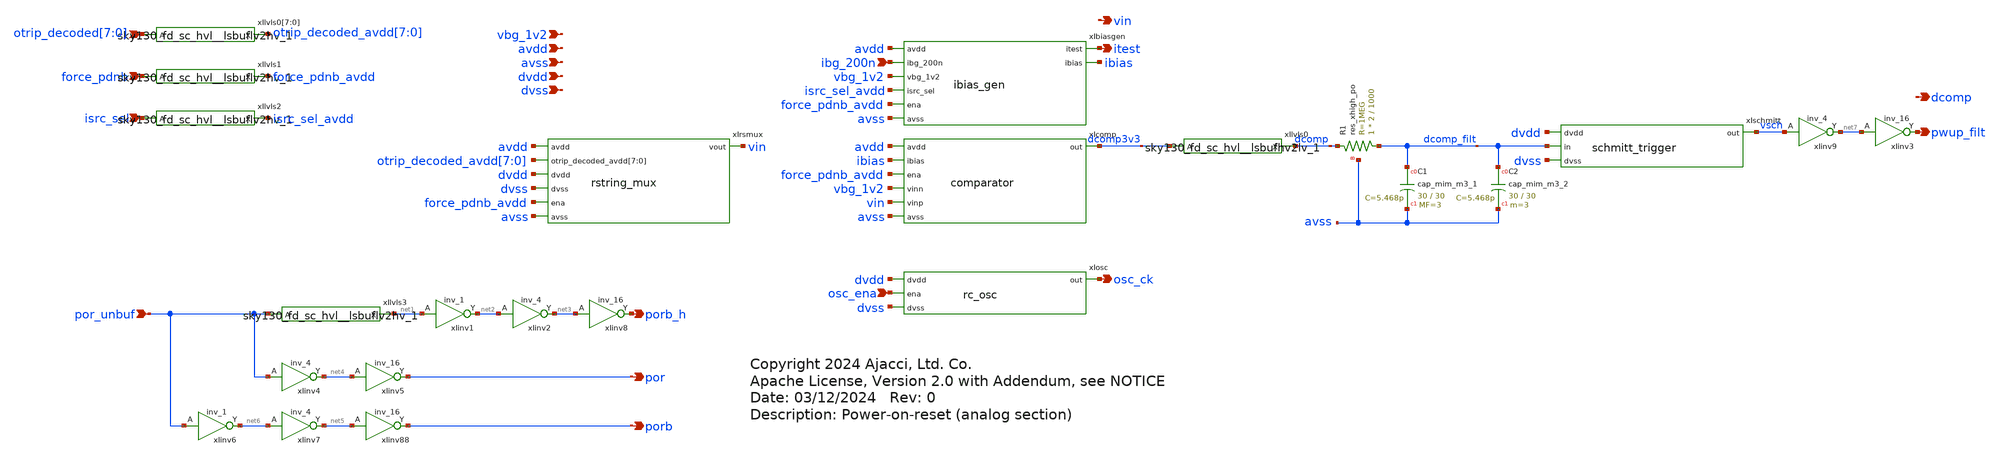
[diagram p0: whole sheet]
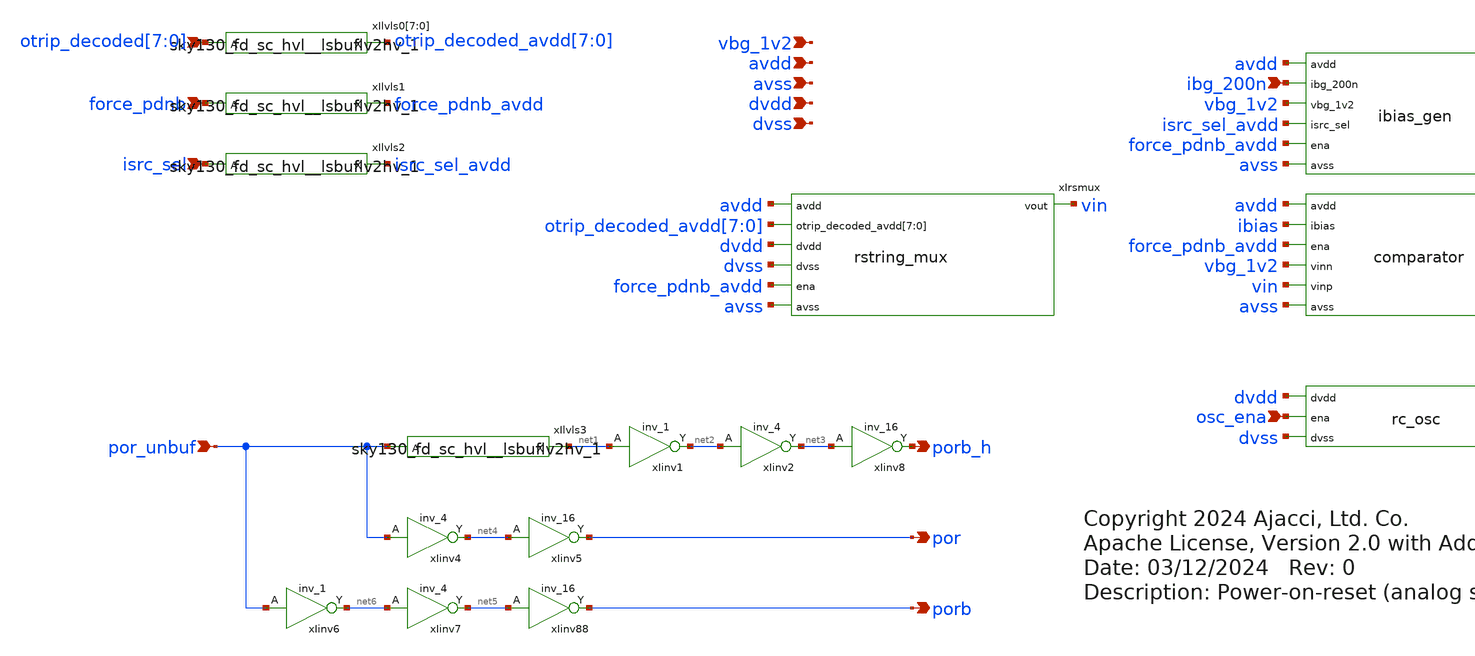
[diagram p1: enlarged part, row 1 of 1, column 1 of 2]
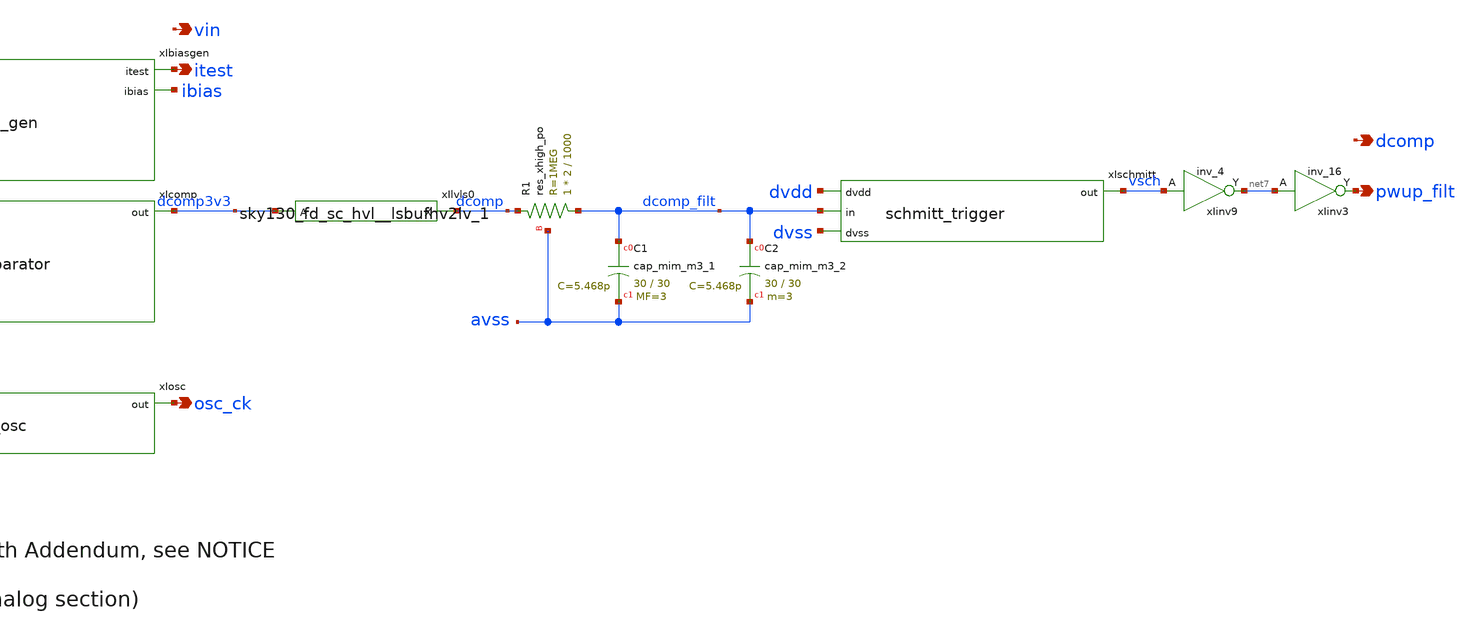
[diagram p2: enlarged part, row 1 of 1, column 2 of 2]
** sch_path: xschem/por_ana.sch
* Copyright 2024 Ajacci, Ltd. Co.
* Apache License, Version 2.0 with Addendum, see NOTICE
**.subckt por_ana vbg_1v2 avdd avss dvdd dvss force_pdnb isrc_sel ibg_200n pwup_filt itest osc_ena
*+ osc_ck
*+ otrip_decoded[7],otrip_decoded[6],otrip_decoded[5],otrip_decoded[4],otrip_decoded[3],otrip_decoded[2],otrip_decoded[1],otrip_decoded[0] vin por_unbuf porb_h por porb dcomp
*.ipin vbg_1v2
*.ipin avdd
*.ipin avss
*.ipin dvdd
*.ipin dvss
*.ipin force_pdnb
*.ipin isrc_sel
*.ipin ibg_200n
*.opin pwup_filt
*.opin itest
*.ipin osc_ena
*.opin osc_ck
*.ipin
*+ otrip_decoded[7],otrip_decoded[6],otrip_decoded[5],otrip_decoded[4],otrip_decoded[3],otrip_decoded[2],otrip_decoded[1],otrip_decoded[0]
*.opin vin
*.ipin por_unbuf
*.opin porb_h
*.opin por
*.opin porb
*.opin dcomp
XR1 dcomp_filt dcomp avss sky130_fd_pr__res_xhigh_po W=2 L=1000 mult=1 m=1
xIlvls0 dcomp3v3 dvdd avss avss avdd avdd dcomp sky130_fd_sc_hvl__lsbufhv2lv_1
XC1 dcomp_filt avss sky130_fd_pr__cap_mim_m3_1 W=30 L=30 MF=3 m=3
XC2 dcomp_filt avss sky130_fd_pr__cap_mim_m3_2 W=30 L=30 MF=3 m=3
xIlvls0[7] otrip_decoded[7] dvdd avss avss avdd avdd otrip_decoded_avdd[7]
+ sky130_fd_sc_hvl__lsbuflv2hv_1
xIlvls0[6] otrip_decoded[6] dvdd avss avss avdd avdd otrip_decoded_avdd[6]
+ sky130_fd_sc_hvl__lsbuflv2hv_1
xIlvls0[5] otrip_decoded[5] dvdd avss avss avdd avdd otrip_decoded_avdd[5]
+ sky130_fd_sc_hvl__lsbuflv2hv_1
xIlvls0[4] otrip_decoded[4] dvdd avss avss avdd avdd otrip_decoded_avdd[4]
+ sky130_fd_sc_hvl__lsbuflv2hv_1
xIlvls0[3] otrip_decoded[3] dvdd avss avss avdd avdd otrip_decoded_avdd[3]
+ sky130_fd_sc_hvl__lsbuflv2hv_1
xIlvls0[2] otrip_decoded[2] dvdd avss avss avdd avdd otrip_decoded_avdd[2]
+ sky130_fd_sc_hvl__lsbuflv2hv_1
xIlvls0[1] otrip_decoded[1] dvdd avss avss avdd avdd otrip_decoded_avdd[1]
+ sky130_fd_sc_hvl__lsbuflv2hv_1
xIlvls0[0] otrip_decoded[0] dvdd avss avss avdd avdd otrip_decoded_avdd[0]
+ sky130_fd_sc_hvl__lsbuflv2hv_1
xIlvls1 force_pdnb dvdd avss avss avdd avdd force_pdnb_avdd sky130_fd_sc_hvl__lsbuflv2hv_1
xIlvls2 isrc_sel dvdd avss avss avdd avdd isrc_sel_avdd sky130_fd_sc_hvl__lsbuflv2hv_1
xIrsmux avdd vin otrip_decoded_avdd[7] otrip_decoded_avdd[6] otrip_decoded_avdd[5]
+ otrip_decoded_avdd[4] otrip_decoded_avdd[3] otrip_decoded_avdd[2] otrip_decoded_avdd[1] otrip_decoded_avdd[0] dvdd dvss
+ force_pdnb_avdd avss rstring_mux
xIcomp avdd ibias dcomp3v3 force_pdnb_avdd vbg_1v2 vin avss comparator
xIbiasgen avdd itest ibias ibg_200n vbg_1v2 isrc_sel_avdd force_pdnb_avdd avss ibias_gen
xIosc dvdd osc_ck osc_ena dvss rc_osc
xIlvls3 por_unbuf dvdd avss avss avdd avdd net1 sky130_fd_sc_hvl__lsbuflv2hv_1
xIinv4 por_unbuf dvss dvss dvdd dvdd net4 sky130_fd_sc_hd__inv_4
xIinv5 net4 dvss dvss dvdd dvdd por sky130_fd_sc_hd__inv_16
xIinv7 net6 dvss dvss dvdd dvdd net5 sky130_fd_sc_hd__inv_4
xIinv88 net5 dvss dvss dvdd dvdd porb sky130_fd_sc_hd__inv_16
xIinv6 por_unbuf dvss dvss dvdd dvdd net6 sky130_fd_sc_hd__inv_1
xIinv8 net3 avss avss avdd avdd porb_h sky130_fd_sc_hvl__inv_16
xIinv2 net2 avss avss avdd avdd net3 sky130_fd_sc_hvl__inv_4
xIinv1 net1 avss avss avdd avdd net2 sky130_fd_sc_hvl__inv_1
xIschmitt dvdd dcomp_filt vsch dvss schmitt_trigger
xIinv3 net7 dvss dvss dvdd dvdd pwup_filt sky130_fd_sc_hd__inv_16
xIinv9 vsch dvss dvss dvdd dvdd net7 sky130_fd_sc_hvl__inv_4
**.ends

* expanding   symbol:  rstring_mux.sym # of pins=7
** sym_path: xschem/rstring_mux.sym
** sch_path: xschem/rstring_mux.sch
.subckt rstring_mux avdd vout otrip_decoded_avdd[7] otrip_decoded_avdd[6] otrip_decoded_avdd[5]
+ otrip_decoded_avdd[4] otrip_decoded_avdd[3] otrip_decoded_avdd[2] otrip_decoded_avdd[1] otrip_decoded_avdd[0] dvdd dvss
+ ena avss
*.ipin avdd
*.ipin avss
*.opin vout
*.ipin
*+ otrip_decoded_avdd[7],otrip_decoded_avdd[6],otrip_decoded_avdd[5],otrip_decoded_avdd[4],otrip_decoded_avdd[3],otrip_decoded_avdd[2],otrip_decoded_avdd[1],otrip_decoded_avdd[0]
*.ipin dvss
*.ipin dvdd
*.ipin ena
XR1 net2 net3 avss sky130_fd_pr__res_xhigh_po W=2 L=50 mult=1 m=1
XR2 net3 net4 avss sky130_fd_pr__res_xhigh_po W=2 L=50 mult=1 m=1
XR0 avss net2 avss sky130_fd_pr__res_xhigh_po W=2 L=50 mult=1 m=1
XR3 net4 net5 avss sky130_fd_pr__res_xhigh_po W=2 L=50 mult=1 m=1
XR4 net5 net6 avss sky130_fd_pr__res_xhigh_po W=2 L=50 mult=1 m=1
XR5 net6 net7 avss sky130_fd_pr__res_xhigh_po W=2 L=50 mult=1 m=1
XR6 net7 net8 avss sky130_fd_pr__res_xhigh_po W=2 L=50 mult=1 m=1
XR7 net8 net9 avss sky130_fd_pr__res_xhigh_po W=2 L=50 mult=1 m=1
XR8 net9 net10 avss sky130_fd_pr__res_xhigh_po W=2 L=50 mult=1 m=1
XR9 net10 net11 avss sky130_fd_pr__res_xhigh_po W=2 L=50 mult=1 m=1
XR10 net11 net12 avss sky130_fd_pr__res_xhigh_po W=2 L=50 mult=1 m=1
XR11 net12 net13 avss sky130_fd_pr__res_xhigh_po W=2 L=50 mult=1 m=1
XR12 net13 net14 avss sky130_fd_pr__res_xhigh_po W=2 L=50 mult=1 m=1
XR13 net14 net15 avss sky130_fd_pr__res_xhigh_po W=2 L=50 mult=1 m=1
XR14 net15 net16 avss sky130_fd_pr__res_xhigh_po W=2 L=50 mult=1 m=1
XR15 net16 net17 avss sky130_fd_pr__res_xhigh_po W=2 L=50 mult=1 m=1
XR16 net17 net18 avss sky130_fd_pr__res_xhigh_po W=2 L=50 mult=1 m=1
XR17 net18 net19 avss sky130_fd_pr__res_xhigh_po W=2 L=50 mult=1 m=1
XR18 net19 net20 avss sky130_fd_pr__res_xhigh_po W=2 L=50 mult=1 m=1
XR19 net20 net21 avss sky130_fd_pr__res_xhigh_po W=2 L=50 mult=1 m=1
XR20 net21 net22 avss sky130_fd_pr__res_xhigh_po W=2 L=50 mult=1 m=1
XR21 net22 net23 avss sky130_fd_pr__res_xhigh_po W=2 L=50 mult=1 m=1
XR22 net23 net24 avss sky130_fd_pr__res_xhigh_po W=2 L=50 mult=1 m=1
XR23 net24 net25 avss sky130_fd_pr__res_xhigh_po W=2 L=50 mult=1 m=1
XR24 net25 net26 avss sky130_fd_pr__res_xhigh_po W=2 L=50 mult=1 m=1
XR25 net26 net27 avss sky130_fd_pr__res_xhigh_po W=2 L=50 mult=1 m=1
XR26 net27 net28 avss sky130_fd_pr__res_xhigh_po W=2 L=50 mult=1 m=1
XR27 net28 vtrip7 avss sky130_fd_pr__res_xhigh_po W=2 L=50 mult=1 m=1
XR28 vtrip7 vtrip6 avss sky130_fd_pr__res_xhigh_po W=2 L=50 mult=1 m=1
XR29 vtrip6 vtrip5 avss sky130_fd_pr__res_xhigh_po W=2 L=50 mult=1 m=1
XR30 vtrip5 vtrip4 avss sky130_fd_pr__res_xhigh_po W=2 L=50 mult=1 m=1
XR31 vtrip4 vtrip3 avss sky130_fd_pr__res_xhigh_po W=2 L=50 mult=1 m=1
XR32 vtrip3 vtrip2 avss sky130_fd_pr__res_xhigh_po W=2 L=50 mult=1 m=1
XR33 vtrip2 vtrip1 avss sky130_fd_pr__res_xhigh_po W=2 L=50 mult=1 m=1
XR34 vtrip1 vtrip0 avss sky130_fd_pr__res_xhigh_po W=2 L=50 mult=1 m=1
XR35 vtrip0 net29 avss sky130_fd_pr__res_xhigh_po W=2 L=50 mult=1 m=1
XR36 net29 net30 avss sky130_fd_pr__res_xhigh_po W=2 L=50 mult=1 m=1
XR37 net30 net31 avss sky130_fd_pr__res_xhigh_po W=2 L=50 mult=1 m=1
XR38 net31 net32 avss sky130_fd_pr__res_xhigh_po W=2 L=50 mult=1 m=1
XR39 net32 net33 avss sky130_fd_pr__res_xhigh_po W=2 L=50 mult=1 m=1
XR40 net33 net34 avss sky130_fd_pr__res_xhigh_po W=2 L=50 mult=1 m=1
XR41 net34 net35 avss sky130_fd_pr__res_xhigh_po W=2 L=50 mult=1 m=1
XR42 net35 net36 avss sky130_fd_pr__res_xhigh_po W=2 L=50 mult=1 m=1
XR43 net36 net37 avss sky130_fd_pr__res_xhigh_po W=2 L=50 mult=1 m=1
XR44 net37 net38 avss sky130_fd_pr__res_xhigh_po W=2 L=50 mult=1 m=1
XR45 net38 net39 avss sky130_fd_pr__res_xhigh_po W=2 L=50 mult=1 m=1
XR46 net39 net40 avss sky130_fd_pr__res_xhigh_po W=2 L=50 mult=1 m=1
XR47 net40 net41 avss sky130_fd_pr__res_xhigh_po W=2 L=50 mult=1 m=1
XR48 net41 net42 avss sky130_fd_pr__res_xhigh_po W=2 L=50 mult=1 m=1
XR49 net42 net43 avss sky130_fd_pr__res_xhigh_po W=2 L=50 mult=1 m=1
XR50 net43 net44 avss sky130_fd_pr__res_xhigh_po W=2 L=50 mult=1 m=1
XR51 net44 net45 avss sky130_fd_pr__res_xhigh_po W=2 L=50 mult=1 m=1
XR52 net45 net46 avss sky130_fd_pr__res_xhigh_po W=2 L=50 mult=1 m=1
XR53 net46 net47 avss sky130_fd_pr__res_xhigh_po W=2 L=50 mult=1 m=1
XR54 net47 net48 avss sky130_fd_pr__res_xhigh_po W=2 L=50 mult=1 m=1
XR55 net48 net49 avss sky130_fd_pr__res_xhigh_po W=2 L=50 mult=1 m=1
XR56 net49 net50 avss sky130_fd_pr__res_xhigh_po W=2 L=50 mult=1 m=1
XR57 net50 net51 avss sky130_fd_pr__res_xhigh_po W=2 L=50 mult=1 m=1
XR58 net51 net52 avss sky130_fd_pr__res_xhigh_po W=2 L=50 mult=1 m=1
XR59 net52 net53 avss sky130_fd_pr__res_xhigh_po W=2 L=50 mult=1 m=1
XR60 net53 net54 avss sky130_fd_pr__res_xhigh_po W=2 L=50 mult=1 m=1
XR61 net54 net55 avss sky130_fd_pr__res_xhigh_po W=2 L=50 mult=1 m=1
XR62 net55 net56 avss sky130_fd_pr__res_xhigh_po W=2 L=50 mult=1 m=1
XR63 net56 net57 avss sky130_fd_pr__res_xhigh_po W=2 L=50 mult=1 m=1
XR64 net57 net58 avss sky130_fd_pr__res_xhigh_po W=2 L=50 mult=1 m=1
XR65 net58 net59 avss sky130_fd_pr__res_xhigh_po W=2 L=50 mult=1 m=1
XR66 net59 net60 avss sky130_fd_pr__res_xhigh_po W=2 L=50 mult=1 m=1
XR67 net60 net61 avss sky130_fd_pr__res_xhigh_po W=2 L=50 mult=1 m=1
XR68 net61 net62 avss sky130_fd_pr__res_xhigh_po W=2 L=50 mult=1 m=1
XR69 net62 net1 avss sky130_fd_pr__res_xhigh_po W=2 L=50 mult=1 m=1
XMtp[7] vtrip7 otrip_decoded_b_avdd[7] vout avdd sky130_fd_pr__pfet_g5v0d10v5 L=0.6 W=5 nf=1 ad='int((nf+1)/2) * W/nf * 0.29'
+ as='int((nf+2)/2) * W/nf * 0.29' pd='2*int((nf+1)/2) * (W/nf + 0.29)' ps='2*int((nf+2)/2) * (W/nf + 0.29)'
+ nrd='0.29 / W' nrs='0.29 / W' sa=0 sb=0 sd=0 mult=2 m=2
XMtp[6] vtrip6 otrip_decoded_b_avdd[6] vout avdd sky130_fd_pr__pfet_g5v0d10v5 L=0.6 W=5 nf=1 ad='int((nf+1)/2) * W/nf * 0.29'
+ as='int((nf+2)/2) * W/nf * 0.29' pd='2*int((nf+1)/2) * (W/nf + 0.29)' ps='2*int((nf+2)/2) * (W/nf + 0.29)'
+ nrd='0.29 / W' nrs='0.29 / W' sa=0 sb=0 sd=0 mult=2 m=2
XMtp[5] vtrip5 otrip_decoded_b_avdd[5] vout avdd sky130_fd_pr__pfet_g5v0d10v5 L=0.6 W=5 nf=1 ad='int((nf+1)/2) * W/nf * 0.29'
+ as='int((nf+2)/2) * W/nf * 0.29' pd='2*int((nf+1)/2) * (W/nf + 0.29)' ps='2*int((nf+2)/2) * (W/nf + 0.29)'
+ nrd='0.29 / W' nrs='0.29 / W' sa=0 sb=0 sd=0 mult=2 m=2
XMtp[4] vtrip4 otrip_decoded_b_avdd[4] vout avdd sky130_fd_pr__pfet_g5v0d10v5 L=0.6 W=5 nf=1 ad='int((nf+1)/2) * W/nf * 0.29'
+ as='int((nf+2)/2) * W/nf * 0.29' pd='2*int((nf+1)/2) * (W/nf + 0.29)' ps='2*int((nf+2)/2) * (W/nf + 0.29)'
+ nrd='0.29 / W' nrs='0.29 / W' sa=0 sb=0 sd=0 mult=2 m=2
XMtp[3] vtrip3 otrip_decoded_b_avdd[3] vout avdd sky130_fd_pr__pfet_g5v0d10v5 L=0.6 W=5 nf=1 ad='int((nf+1)/2) * W/nf * 0.29'
+ as='int((nf+2)/2) * W/nf * 0.29' pd='2*int((nf+1)/2) * (W/nf + 0.29)' ps='2*int((nf+2)/2) * (W/nf + 0.29)'
+ nrd='0.29 / W' nrs='0.29 / W' sa=0 sb=0 sd=0 mult=2 m=2
XMtp[2] vtrip2 otrip_decoded_b_avdd[2] vout avdd sky130_fd_pr__pfet_g5v0d10v5 L=0.6 W=5 nf=1 ad='int((nf+1)/2) * W/nf * 0.29'
+ as='int((nf+2)/2) * W/nf * 0.29' pd='2*int((nf+1)/2) * (W/nf + 0.29)' ps='2*int((nf+2)/2) * (W/nf + 0.29)'
+ nrd='0.29 / W' nrs='0.29 / W' sa=0 sb=0 sd=0 mult=2 m=2
XMtp[1] vtrip1 otrip_decoded_b_avdd[1] vout avdd sky130_fd_pr__pfet_g5v0d10v5 L=0.6 W=5 nf=1 ad='int((nf+1)/2) * W/nf * 0.29'
+ as='int((nf+2)/2) * W/nf * 0.29' pd='2*int((nf+1)/2) * (W/nf + 0.29)' ps='2*int((nf+2)/2) * (W/nf + 0.29)'
+ nrd='0.29 / W' nrs='0.29 / W' sa=0 sb=0 sd=0 mult=2 m=2
XMtp[0] vtrip0 otrip_decoded_b_avdd[0] vout avdd sky130_fd_pr__pfet_g5v0d10v5 L=0.6 W=5 nf=1 ad='int((nf+1)/2) * W/nf * 0.29'
+ as='int((nf+2)/2) * W/nf * 0.29' pd='2*int((nf+1)/2) * (W/nf + 0.29)' ps='2*int((nf+2)/2) * (W/nf + 0.29)'
+ nrd='0.29 / W' nrs='0.29 / W' sa=0 sb=0 sd=0 mult=2 m=2
XMtn[7] vout otrip_decoded_avdd[7] vtrip7 avss sky130_fd_pr__nfet_g5v0d10v5 L=0.6 W=5 nf=1 ad='int((nf+1)/2) * W/nf * 0.29'
+ as='int((nf+2)/2) * W/nf * 0.29' pd='2*int((nf+1)/2) * (W/nf + 0.29)' ps='2*int((nf+2)/2) * (W/nf + 0.29)'
+ nrd='0.29 / W' nrs='0.29 / W' sa=0 sb=0 sd=0 mult=2 m=2
XMtn[6] vout otrip_decoded_avdd[6] vtrip6 avss sky130_fd_pr__nfet_g5v0d10v5 L=0.6 W=5 nf=1 ad='int((nf+1)/2) * W/nf * 0.29'
+ as='int((nf+2)/2) * W/nf * 0.29' pd='2*int((nf+1)/2) * (W/nf + 0.29)' ps='2*int((nf+2)/2) * (W/nf + 0.29)'
+ nrd='0.29 / W' nrs='0.29 / W' sa=0 sb=0 sd=0 mult=2 m=2
XMtn[5] vout otrip_decoded_avdd[5] vtrip5 avss sky130_fd_pr__nfet_g5v0d10v5 L=0.6 W=5 nf=1 ad='int((nf+1)/2) * W/nf * 0.29'
+ as='int((nf+2)/2) * W/nf * 0.29' pd='2*int((nf+1)/2) * (W/nf + 0.29)' ps='2*int((nf+2)/2) * (W/nf + 0.29)'
+ nrd='0.29 / W' nrs='0.29 / W' sa=0 sb=0 sd=0 mult=2 m=2
XMtn[4] vout otrip_decoded_avdd[4] vtrip4 avss sky130_fd_pr__nfet_g5v0d10v5 L=0.6 W=5 nf=1 ad='int((nf+1)/2) * W/nf * 0.29'
+ as='int((nf+2)/2) * W/nf * 0.29' pd='2*int((nf+1)/2) * (W/nf + 0.29)' ps='2*int((nf+2)/2) * (W/nf + 0.29)'
+ nrd='0.29 / W' nrs='0.29 / W' sa=0 sb=0 sd=0 mult=2 m=2
XMtn[3] vout otrip_decoded_avdd[3] vtrip3 avss sky130_fd_pr__nfet_g5v0d10v5 L=0.6 W=5 nf=1 ad='int((nf+1)/2) * W/nf * 0.29'
+ as='int((nf+2)/2) * W/nf * 0.29' pd='2*int((nf+1)/2) * (W/nf + 0.29)' ps='2*int((nf+2)/2) * (W/nf + 0.29)'
+ nrd='0.29 / W' nrs='0.29 / W' sa=0 sb=0 sd=0 mult=2 m=2
XMtn[2] vout otrip_decoded_avdd[2] vtrip2 avss sky130_fd_pr__nfet_g5v0d10v5 L=0.6 W=5 nf=1 ad='int((nf+1)/2) * W/nf * 0.29'
+ as='int((nf+2)/2) * W/nf * 0.29' pd='2*int((nf+1)/2) * (W/nf + 0.29)' ps='2*int((nf+2)/2) * (W/nf + 0.29)'
+ nrd='0.29 / W' nrs='0.29 / W' sa=0 sb=0 sd=0 mult=2 m=2
XMtn[1] vout otrip_decoded_avdd[1] vtrip1 avss sky130_fd_pr__nfet_g5v0d10v5 L=0.6 W=5 nf=1 ad='int((nf+1)/2) * W/nf * 0.29'
+ as='int((nf+2)/2) * W/nf * 0.29' pd='2*int((nf+1)/2) * (W/nf + 0.29)' ps='2*int((nf+2)/2) * (W/nf + 0.29)'
+ nrd='0.29 / W' nrs='0.29 / W' sa=0 sb=0 sd=0 mult=2 m=2
XMtn[0] vout otrip_decoded_avdd[0] vtrip0 avss sky130_fd_pr__nfet_g5v0d10v5 L=0.6 W=5 nf=1 ad='int((nf+1)/2) * W/nf * 0.29'
+ as='int((nf+2)/2) * W/nf * 0.29' pd='2*int((nf+1)/2) * (W/nf + 0.29)' ps='2*int((nf+2)/2) * (W/nf + 0.29)'
+ nrd='0.29 / W' nrs='0.29 / W' sa=0 sb=0 sd=0 mult=2 m=2
XMpdn net1 ena_b avss avss sky130_fd_pr__nfet_g5v0d10v5 L=1 W=1 nf=1 ad='int((nf+1)/2) * W/nf * 0.29'
+ as='int((nf+2)/2) * W/nf * 0.29' pd='2*int((nf+1)/2) * (W/nf + 0.29)' ps='2*int((nf+2)/2) * (W/nf + 0.29)'
+ nrd='0.29 / W' nrs='0.29 / W' sa=0 sb=0 sd=0 mult=1 m=1
xIinv0[7] otrip_decoded_avdd[7] avss avss avdd avdd otrip_decoded_b_avdd[7] sky130_fd_sc_hvl__inv_1
xIinv0[6] otrip_decoded_avdd[6] avss avss avdd avdd otrip_decoded_b_avdd[6] sky130_fd_sc_hvl__inv_1
xIinv0[5] otrip_decoded_avdd[5] avss avss avdd avdd otrip_decoded_b_avdd[5] sky130_fd_sc_hvl__inv_1
xIinv0[4] otrip_decoded_avdd[4] avss avss avdd avdd otrip_decoded_b_avdd[4] sky130_fd_sc_hvl__inv_1
xIinv0[3] otrip_decoded_avdd[3] avss avss avdd avdd otrip_decoded_b_avdd[3] sky130_fd_sc_hvl__inv_1
xIinv0[2] otrip_decoded_avdd[2] avss avss avdd avdd otrip_decoded_b_avdd[2] sky130_fd_sc_hvl__inv_1
xIinv0[1] otrip_decoded_avdd[1] avss avss avdd avdd otrip_decoded_b_avdd[1] sky130_fd_sc_hvl__inv_1
xIinv0[0] otrip_decoded_avdd[0] avss avss avdd avdd otrip_decoded_b_avdd[0] sky130_fd_sc_hvl__inv_1
xIinv1 ena avss avss avdd avdd ena_b sky130_fd_sc_hvl__inv_1
XMpdp avdd ena_b net1 avdd sky130_fd_pr__pfet_g5v0d10v5 L=0.6 W=5 nf=1 ad='int((nf+1)/2) * W/nf * 0.29'
+ as='int((nf+2)/2) * W/nf * 0.29' pd='2*int((nf+1)/2) * (W/nf + 0.29)' ps='2*int((nf+2)/2) * (W/nf + 0.29)'
+ nrd='0.29 / W' nrs='0.29 / W' sa=0 sb=0 sd=0 mult=16 m=16
.ends


* expanding   symbol:  comparator.sym # of pins=7
** sym_path: xschem/comparator.sym
** sch_path: xschem/comparator.sch
.subckt comparator avdd ibias out ena vinn vinp avss
*.ipin ena
*.ipin avdd
*.ipin avss
*.ipin ibias
*.ipin vinn
*.ipin vinp
*.opin out
XMb vn vn avss avss sky130_fd_pr__nfet_g5v0d10v5 L=8 W=1 nf=1 ad='int((nf+1)/2) * W/nf * 0.29' as='int((nf+2)/2) * W/nf * 0.29'
+ pd='2*int((nf+1)/2) * (W/nf + 0.29)' ps='2*int((nf+2)/2) * (W/nf + 0.29)' nrd='0.29 / W' nrs='0.29 / W'
+ sa=0 sb=0 sd=0 mult=2 m=2
XMta vt vn avss avss sky130_fd_pr__nfet_g5v0d10v5 L=8 W=1 nf=1 ad='int((nf+1)/2) * W/nf * 0.29' as='int((nf+2)/2) * W/nf * 0.29'
+ pd='2*int((nf+1)/2) * (W/nf + 0.29)' ps='2*int((nf+2)/2) * (W/nf + 0.29)' nrd='0.29 / W' nrs='0.29 / W'
+ sa=0 sb=0 sd=0 mult=2 m=2
XMl0 vn ena_b avss avss sky130_fd_pr__nfet_g5v0d10v5 L=1 W=1 nf=1 ad='int((nf+1)/2) * W/nf * 0.29' as='int((nf+2)/2) * W/nf * 0.29'
+ pd='2*int((nf+1)/2) * (W/nf + 0.29)' ps='2*int((nf+2)/2) * (W/nf + 0.29)' nrd='0.29 / W' nrs='0.29 / W'
+ sa=0 sb=0 sd=0 mult=1 m=1
XMinv0 ena_b ena avss avss sky130_fd_pr__nfet_g5v0d10v5 L=1 W=1 nf=1 ad='int((nf+1)/2) * W/nf * 0.29'
+ as='int((nf+2)/2) * W/nf * 0.29' pd='2*int((nf+1)/2) * (W/nf + 0.29)' ps='2*int((nf+2)/2) * (W/nf + 0.29)'
+ nrd='0.29 / W' nrs='0.29 / W' sa=0 sb=0 sd=0 mult=1 m=1
XMinv1 ena_b ena avdd avdd sky130_fd_pr__pfet_g5v0d10v5 L=1 W=1 nf=1 ad='int((nf+1)/2) * W/nf * 0.29'
+ as='int((nf+2)/2) * W/nf * 0.29' pd='2*int((nf+1)/2) * (W/nf + 0.29)' ps='2*int((nf+2)/2) * (W/nf + 0.29)'
+ nrd='0.29 / W' nrs='0.29 / W' sa=0 sb=0 sd=0 mult=1 m=1
XMi0 vnn vinn vt vt sky130_fd_pr__nfet_g5v0d10v5 L=8 W=0.42 nf=1 ad='int((nf+1)/2) * W/nf * 0.29' as='int((nf+2)/2) * W/nf * 0.29'
+ pd='2*int((nf+1)/2) * (W/nf + 0.29)' ps='2*int((nf+2)/2) * (W/nf + 0.29)' nrd='0.29 / W' nrs='0.29 / W'
+ sa=0 sb=0 sd=0 mult=16 m=16
XMi1 vpp vinp vt vt sky130_fd_pr__nfet_g5v0d10v5 L=8 W=0.42 nf=1 ad='int((nf+1)/2) * W/nf * 0.29' as='int((nf+2)/2) * W/nf * 0.29'
+ pd='2*int((nf+1)/2) * (W/nf + 0.29)' ps='2*int((nf+2)/2) * (W/nf + 0.29)' nrd='0.29 / W' nrs='0.29 / W'
+ sa=0 sb=0 sd=0 mult=16 m=16
XMld1 vpp vpp avdd avdd sky130_fd_pr__pfet_g5v0d10v5 L=8 W=0.42 nf=1 ad='int((nf+1)/2) * W/nf * 0.29'
+ as='int((nf+2)/2) * W/nf * 0.29' pd='2*int((nf+1)/2) * (W/nf + 0.29)' ps='2*int((nf+2)/2) * (W/nf + 0.29)'
+ nrd='0.29 / W' nrs='0.29 / W' sa=0 sb=0 sd=0 mult=8 m=8
XMh1 vnn vpp avdd avdd sky130_fd_pr__pfet_g5v0d10v5 L=8 W=0.42 nf=1 ad='int((nf+1)/2) * W/nf * 0.29'
+ as='int((nf+2)/2) * W/nf * 0.29' pd='2*int((nf+1)/2) * (W/nf + 0.29)' ps='2*int((nf+2)/2) * (W/nf + 0.29)'
+ nrd='0.29 / W' nrs='0.29 / W' sa=0 sb=0 sd=0 mult=14 m=14
XMh0 vpp vnn avdd avdd sky130_fd_pr__pfet_g5v0d10v5 L=8 W=0.42 nf=1 ad='int((nf+1)/2) * W/nf * 0.29'
+ as='int((nf+2)/2) * W/nf * 0.29' pd='2*int((nf+1)/2) * (W/nf + 0.29)' ps='2*int((nf+2)/2) * (W/nf + 0.29)'
+ nrd='0.29 / W' nrs='0.29 / W' sa=0 sb=0 sd=0 mult=14 m=14
XMld0 vnn vnn avdd avdd sky130_fd_pr__pfet_g5v0d10v5 L=8 W=0.42 nf=1 ad='int((nf+1)/2) * W/nf * 0.29'
+ as='int((nf+2)/2) * W/nf * 0.29' pd='2*int((nf+1)/2) * (W/nf + 0.29)' ps='2*int((nf+2)/2) * (W/nf + 0.29)'
+ nrd='0.29 / W' nrs='0.29 / W' sa=0 sb=0 sd=0 mult=8 m=8
XMpp1 n0 vpp avdd avdd sky130_fd_pr__pfet_g5v0d10v5 L=8 W=1 nf=1 ad='int((nf+1)/2) * W/nf * 0.29' as='int((nf+2)/2) * W/nf * 0.29'
+ pd='2*int((nf+1)/2) * (W/nf + 0.29)' ps='2*int((nf+2)/2) * (W/nf + 0.29)' nrd='0.29 / W' nrs='0.29 / W'
+ sa=0 sb=0 sd=0 mult=2 m=2
XMnn1 n0 vm avss avss sky130_fd_pr__nfet_g5v0d10v5 L=8 W=1 nf=1 ad='int((nf+1)/2) * W/nf * 0.29' as='int((nf+2)/2) * W/nf * 0.29'
+ pd='2*int((nf+1)/2) * (W/nf + 0.29)' ps='2*int((nf+2)/2) * (W/nf + 0.29)' nrd='0.29 / W' nrs='0.29 / W'
+ sa=0 sb=0 sd=0 mult=2 m=2
XMpp0 vm vnn avdd avdd sky130_fd_pr__pfet_g5v0d10v5 L=8 W=1 nf=1 ad='int((nf+1)/2) * W/nf * 0.29' as='int((nf+2)/2) * W/nf * 0.29'
+ pd='2*int((nf+1)/2) * (W/nf + 0.29)' ps='2*int((nf+2)/2) * (W/nf + 0.29)' nrd='0.29 / W' nrs='0.29 / W'
+ sa=0 sb=0 sd=0 mult=2 m=2
XMnn0 vm vm avss avss sky130_fd_pr__nfet_g5v0d10v5 L=8 W=1 nf=1 ad='int((nf+1)/2) * W/nf * 0.29' as='int((nf+2)/2) * W/nf * 0.29'
+ pd='2*int((nf+1)/2) * (W/nf + 0.29)' ps='2*int((nf+2)/2) * (W/nf + 0.29)' nrd='0.29 / W' nrs='0.29 / W'
+ sa=0 sb=0 sd=0 mult=2 m=2
XMinv3 n1 n0 avdd avdd sky130_fd_pr__pfet_g5v0d10v5 L=0.6 W=1 nf=1 ad='int((nf+1)/2) * W/nf * 0.29' as='int((nf+2)/2) * W/nf * 0.29'
+ pd='2*int((nf+1)/2) * (W/nf + 0.29)' ps='2*int((nf+2)/2) * (W/nf + 0.29)' nrd='0.29 / W' nrs='0.29 / W'
+ sa=0 sb=0 sd=0 mult=2 m=2
XMinv2 n1 n0 avss avss sky130_fd_pr__nfet_g5v0d10v5 L=0.6 W=1 nf=1 ad='int((nf+1)/2) * W/nf * 0.29' as='int((nf+2)/2) * W/nf * 0.29'
+ pd='2*int((nf+1)/2) * (W/nf + 0.29)' ps='2*int((nf+2)/2) * (W/nf + 0.29)' nrd='0.29 / W' nrs='0.29 / W'
+ sa=0 sb=0 sd=0 mult=2 m=2
XMinv5 out n1 avdd avdd sky130_fd_pr__pfet_g5v0d10v5 L=0.6 W=1 nf=1 ad='int((nf+1)/2) * W/nf * 0.29'
+ as='int((nf+2)/2) * W/nf * 0.29' pd='2*int((nf+1)/2) * (W/nf + 0.29)' ps='2*int((nf+2)/2) * (W/nf + 0.29)'
+ nrd='0.29 / W' nrs='0.29 / W' sa=0 sb=0 sd=0 mult=8 m=8
XMinv4 out n1 avss avss sky130_fd_pr__nfet_g5v0d10v5 L=0.6 W=1 nf=1 ad='int((nf+1)/2) * W/nf * 0.29'
+ as='int((nf+2)/2) * W/nf * 0.29' pd='2*int((nf+1)/2) * (W/nf + 0.29)' ps='2*int((nf+2)/2) * (W/nf + 0.29)'
+ nrd='0.29 / W' nrs='0.29 / W' sa=0 sb=0 sd=0 mult=8 m=8
XMl1 vm ena_b avss avss sky130_fd_pr__nfet_g5v0d10v5 L=1 W=1 nf=1 ad='int((nf+1)/2) * W/nf * 0.29' as='int((nf+2)/2) * W/nf * 0.29'
+ pd='2*int((nf+1)/2) * (W/nf + 0.29)' ps='2*int((nf+2)/2) * (W/nf + 0.29)' nrd='0.29 / W' nrs='0.29 / W'
+ sa=0 sb=0 sd=0 mult=1 m=1
XMl3 vnn ena avdd avdd sky130_fd_pr__pfet_g5v0d10v5 L=1 W=1 nf=1 ad='int((nf+1)/2) * W/nf * 0.29' as='int((nf+2)/2) * W/nf * 0.29'
+ pd='2*int((nf+1)/2) * (W/nf + 0.29)' ps='2*int((nf+2)/2) * (W/nf + 0.29)' nrd='0.29 / W' nrs='0.29 / W'
+ sa=0 sb=0 sd=0 mult=1 m=1
XMl4 vpp ena avdd avdd sky130_fd_pr__pfet_g5v0d10v5 L=1 W=1 nf=1 ad='int((nf+1)/2) * W/nf * 0.29' as='int((nf+2)/2) * W/nf * 0.29'
+ pd='2*int((nf+1)/2) * (W/nf + 0.29)' ps='2*int((nf+2)/2) * (W/nf + 0.29)' nrd='0.29 / W' nrs='0.29 / W'
+ sa=0 sb=0 sd=0 mult=1 m=1
XMt1 ibias ena vn avss sky130_fd_pr__nfet_g5v0d10v5 L=1 W=1 nf=1 ad='int((nf+1)/2) * W/nf * 0.29' as='int((nf+2)/2) * W/nf * 0.29'
+ pd='2*int((nf+1)/2) * (W/nf + 0.29)' ps='2*int((nf+2)/2) * (W/nf + 0.29)' nrd='0.29 / W' nrs='0.29 / W'
+ sa=0 sb=0 sd=0 mult=1 m=1
XMt0 vn ena_b ibias avdd sky130_fd_pr__pfet_g5v0d10v5 L=1 W=1 nf=1 ad='int((nf+1)/2) * W/nf * 0.29' as='int((nf+2)/2) * W/nf * 0.29'
+ pd='2*int((nf+1)/2) * (W/nf + 0.29)' ps='2*int((nf+2)/2) * (W/nf + 0.29)' nrd='0.29 / W' nrs='0.29 / W'
+ sa=0 sb=0 sd=0 mult=1 m=1
XMl2 n0 ena_b avss avss sky130_fd_pr__nfet_g5v0d10v5 L=1 W=1 nf=1 ad='int((nf+1)/2) * W/nf * 0.29' as='int((nf+2)/2) * W/nf * 0.29'
+ pd='2*int((nf+1)/2) * (W/nf + 0.29)' ps='2*int((nf+2)/2) * (W/nf + 0.29)' nrd='0.29 / W' nrs='0.29 / W'
+ sa=0 sb=0 sd=0 mult=1 m=1
.ends


* expanding   symbol:  ibias_gen.sym # of pins=8
** sym_path: xschem/ibias_gen.sym
** sch_path: xschem/ibias_gen.sch
.subckt ibias_gen avdd itest ibias ibg_200n vbg_1v2 isrc_sel ena avss
*.ipin vbg_1v2
*.ipin ena
*.opin ibias
*.ipin ibg_200n
*.ipin isrc_sel
*.ipin avdd
*.ipin avss
*.opin itest
XR1 avss net3 avss sky130_fd_pr__res_xhigh_po W=2 L=1000 mult=1 m=1
XQ1 avss avss net2 sky130_fd_pr__pnp_05v5_W0p68L0p68 m=1
XM17 net1 vbg_1v2 vn0 avss sky130_fd_pr__nfet_g5v0d10v5 L=0.6 W=5 nf=1 ad='int((nf+1)/2) * W/nf * 0.29'
+ as='int((nf+2)/2) * W/nf * 0.29' pd='2*int((nf+1)/2) * (W/nf + 0.29)' ps='2*int((nf+2)/2) * (W/nf + 0.29)'
+ nrd='0.29 / W' nrs='0.29 / W' sa=0 sb=0 sd=0 mult=10 m=10
XMt9 net1 ena_b net4 avdd sky130_fd_pr__pfet_g5v0d10v5 L=0.6 W=5 nf=1 ad='int((nf+1)/2) * W/nf * 0.29'
+ as='int((nf+2)/2) * W/nf * 0.29' pd='2*int((nf+1)/2) * (W/nf + 0.29)' ps='2*int((nf+2)/2) * (W/nf + 0.29)'
+ nrd='0.29 / W' nrs='0.29 / W' sa=0 sb=0 sd=0 mult=1 m=1
XMn0 vn0 vn0 net2 avss sky130_fd_pr__nfet_g5v0d10v5 L=4 W=5 nf=1 ad='int((nf+1)/2) * W/nf * 0.29' as='int((nf+2)/2) * W/nf * 0.29'
+ pd='2*int((nf+1)/2) * (W/nf + 0.29)' ps='2*int((nf+2)/2) * (W/nf + 0.29)' nrd='0.29 / W' nrs='0.29 / W'
+ sa=0 sb=0 sd=0 mult=2 m=2
XMp0 vn0 vp0 avdd avdd sky130_fd_pr__pfet_g5v0d10v5 L=4 W=5 nf=1 ad='int((nf+1)/2) * W/nf * 0.29' as='int((nf+2)/2) * W/nf * 0.29'
+ pd='2*int((nf+1)/2) * (W/nf + 0.29)' ps='2*int((nf+2)/2) * (W/nf + 0.29)' nrd='0.29 / W' nrs='0.29 / W'
+ sa=0 sb=0 sd=0 mult=2 m=2
XMn1 vp0 vn0 net3 avss sky130_fd_pr__nfet_g5v0d10v5 L=4 W=5 nf=1 ad='int((nf+1)/2) * W/nf * 0.29' as='int((nf+2)/2) * W/nf * 0.29'
+ pd='2*int((nf+1)/2) * (W/nf + 0.29)' ps='2*int((nf+2)/2) * (W/nf + 0.29)' nrd='0.29 / W' nrs='0.29 / W'
+ sa=0 sb=0 sd=0 mult=2 m=2
XMp1 vp0 vp0 avdd avdd sky130_fd_pr__pfet_g5v0d10v5 L=4 W=5 nf=1 ad='int((nf+1)/2) * W/nf * 0.29' as='int((nf+2)/2) * W/nf * 0.29'
+ pd='2*int((nf+1)/2) * (W/nf + 0.29)' ps='2*int((nf+2)/2) * (W/nf + 0.29)' nrd='0.29 / W' nrs='0.29 / W'
+ sa=0 sb=0 sd=0 mult=2 m=2
XMp ibias vp avdd avdd sky130_fd_pr__pfet_g5v0d10v5 L=4 W=5 nf=1 ad='int((nf+1)/2) * W/nf * 0.29' as='int((nf+2)/2) * W/nf * 0.29'
+ pd='2*int((nf+1)/2) * (W/nf + 0.29)' ps='2*int((nf+2)/2) * (W/nf + 0.29)' nrd='0.29 / W' nrs='0.29 / W'
+ sa=0 sb=0 sd=0 mult=2 m=2
XMt0 vp0 isrc_sel vp avdd sky130_fd_pr__pfet_g5v0d10v5 L=0.6 W=5 nf=1 ad='int((nf+1)/2) * W/nf * 0.29'
+ as='int((nf+2)/2) * W/nf * 0.29' pd='2*int((nf+1)/2) * (W/nf + 0.29)' ps='2*int((nf+2)/2) * (W/nf + 0.29)'
+ nrd='0.29 / W' nrs='0.29 / W' sa=0 sb=0 sd=0 mult=1 m=1
XMt1 vp isrc_sel_b vp0 avss sky130_fd_pr__nfet_g5v0d10v5 L=0.6 W=5 nf=1 ad='int((nf+1)/2) * W/nf * 0.29'
+ as='int((nf+2)/2) * W/nf * 0.29' pd='2*int((nf+1)/2) * (W/nf + 0.29)' ps='2*int((nf+2)/2) * (W/nf + 0.29)'
+ nrd='0.29 / W' nrs='0.29 / W' sa=0 sb=0 sd=0 mult=1 m=1
XMl6 vp ena avdd avdd sky130_fd_pr__pfet_g5v0d10v5 L=2 W=5 nf=1 ad='int((nf+1)/2) * W/nf * 0.29' as='int((nf+2)/2) * W/nf * 0.29'
+ pd='2*int((nf+1)/2) * (W/nf + 0.29)' ps='2*int((nf+2)/2) * (W/nf + 0.29)' nrd='0.29 / W' nrs='0.29 / W'
+ sa=0 sb=0 sd=0 mult=1 m=1
XMl3 vp0 ena avdd avdd sky130_fd_pr__pfet_g5v0d10v5 L=2 W=5 nf=1 ad='int((nf+1)/2) * W/nf * 0.29' as='int((nf+2)/2) * W/nf * 0.29'
+ pd='2*int((nf+1)/2) * (W/nf + 0.29)' ps='2*int((nf+2)/2) * (W/nf + 0.29)' nrd='0.29 / W' nrs='0.29 / W'
+ sa=0 sb=0 sd=0 mult=1 m=1
XMl1 vn0 ena_b avss avss sky130_fd_pr__nfet_g5v0d10v5 L=2 W=5 nf=1 ad='int((nf+1)/2) * W/nf * 0.29' as='int((nf+2)/2) * W/nf * 0.29'
+ pd='2*int((nf+1)/2) * (W/nf + 0.29)' ps='2*int((nf+2)/2) * (W/nf + 0.29)' nrd='0.29 / W' nrs='0.29 / W'
+ sa=0 sb=0 sd=0 mult=1 m=1
XMnn1 vp1 vn1 avss avss sky130_fd_pr__nfet_g5v0d10v5 L=8 W=5 nf=1 ad='int((nf+1)/2) * W/nf * 0.29' as='int((nf+2)/2) * W/nf * 0.29'
+ pd='2*int((nf+1)/2) * (W/nf + 0.29)' ps='2*int((nf+2)/2) * (W/nf + 0.29)' nrd='0.29 / W' nrs='0.29 / W'
+ sa=0 sb=0 sd=0 mult=8 m=8
XMnn0 vn1 vn1 avss avss sky130_fd_pr__nfet_g5v0d10v5 L=8 W=5 nf=1 ad='int((nf+1)/2) * W/nf * 0.29' as='int((nf+2)/2) * W/nf * 0.29'
+ pd='2*int((nf+1)/2) * (W/nf + 0.29)' ps='2*int((nf+2)/2) * (W/nf + 0.29)' nrd='0.29 / W' nrs='0.29 / W'
+ sa=0 sb=0 sd=0 mult=2 m=2
XMl9 vn1 isrc_sel_b avss avss sky130_fd_pr__nfet_g5v0d10v5 L=2 W=5 nf=1 ad='int((nf+1)/2) * W/nf * 0.29'
+ as='int((nf+2)/2) * W/nf * 0.29' pd='2*int((nf+1)/2) * (W/nf + 0.29)' ps='2*int((nf+2)/2) * (W/nf + 0.29)'
+ nrd='0.29 / W' nrs='0.29 / W' sa=0 sb=0 sd=0 mult=1 m=1
XMt6 net5 isrc_sel vn1 avss sky130_fd_pr__nfet_g5v0d10v5 L=0.6 W=5 nf=1 ad='int((nf+1)/2) * W/nf * 0.29'
+ as='int((nf+2)/2) * W/nf * 0.29' pd='2*int((nf+1)/2) * (W/nf + 0.29)' ps='2*int((nf+2)/2) * (W/nf + 0.29)'
+ nrd='0.29 / W' nrs='0.29 / W' sa=0 sb=0 sd=0 mult=1 m=1
XMt7 vn1 isrc_sel_b net6 avdd sky130_fd_pr__pfet_g5v0d10v5 L=0.6 W=5 nf=1 ad='int((nf+1)/2) * W/nf * 0.29'
+ as='int((nf+2)/2) * W/nf * 0.29' pd='2*int((nf+1)/2) * (W/nf + 0.29)' ps='2*int((nf+2)/2) * (W/nf + 0.29)'
+ nrd='0.29 / W' nrs='0.29 / W' sa=0 sb=0 sd=0 mult=1 m=1
XMpp1 vp1 vp1 avdd avdd sky130_fd_pr__pfet_g5v0d10v5 L=4 W=5 nf=1 ad='int((nf+1)/2) * W/nf * 0.29' as='int((nf+2)/2) * W/nf * 0.29'
+ pd='2*int((nf+1)/2) * (W/nf + 0.29)' ps='2*int((nf+2)/2) * (W/nf + 0.29)' nrd='0.29 / W' nrs='0.29 / W'
+ sa=0 sb=0 sd=0 mult=2 m=2
XMt2 vp isrc_sel_b vp1 avdd sky130_fd_pr__pfet_g5v0d10v5 L=0.6 W=5 nf=1 ad='int((nf+1)/2) * W/nf * 0.29'
+ as='int((nf+2)/2) * W/nf * 0.29' pd='2*int((nf+1)/2) * (W/nf + 0.29)' ps='2*int((nf+2)/2) * (W/nf + 0.29)'
+ nrd='0.29 / W' nrs='0.29 / W' sa=0 sb=0 sd=0 mult=1 m=1
XMt3 vp1 isrc_sel vp avss sky130_fd_pr__nfet_g5v0d10v5 L=0.6 W=5 nf=1 ad='int((nf+1)/2) * W/nf * 0.29'
+ as='int((nf+2)/2) * W/nf * 0.29' pd='2*int((nf+1)/2) * (W/nf + 0.29)' ps='2*int((nf+2)/2) * (W/nf + 0.29)'
+ nrd='0.29 / W' nrs='0.29 / W' sa=0 sb=0 sd=0 mult=1 m=1
XMt4 ibg_200n ena net5 avss sky130_fd_pr__nfet_g5v0d10v5 L=0.6 W=5 nf=1 ad='int((nf+1)/2) * W/nf * 0.29'
+ as='int((nf+2)/2) * W/nf * 0.29' pd='2*int((nf+1)/2) * (W/nf + 0.29)' ps='2*int((nf+2)/2) * (W/nf + 0.29)'
+ nrd='0.29 / W' nrs='0.29 / W' sa=0 sb=0 sd=0 mult=1 m=1
XMt5 net6 ena_b ibg_200n avdd sky130_fd_pr__pfet_g5v0d10v5 L=0.6 W=5 nf=1 ad='int((nf+1)/2) * W/nf * 0.29'
+ as='int((nf+2)/2) * W/nf * 0.29' pd='2*int((nf+1)/2) * (W/nf + 0.29)' ps='2*int((nf+2)/2) * (W/nf + 0.29)'
+ nrd='0.29 / W' nrs='0.29 / W' sa=0 sb=0 sd=0 mult=1 m=1
XMl7 vp1 isrc_sel avdd avdd sky130_fd_pr__pfet_g5v0d10v5 L=2 W=5 nf=1 ad='int((nf+1)/2) * W/nf * 0.29'
+ as='int((nf+2)/2) * W/nf * 0.29' pd='2*int((nf+1)/2) * (W/nf + 0.29)' ps='2*int((nf+2)/2) * (W/nf + 0.29)'
+ nrd='0.29 / W' nrs='0.29 / W' sa=0 sb=0 sd=0 mult=1 m=1
XMl8 vp1 ena avdd avdd sky130_fd_pr__pfet_g5v0d10v5 L=2 W=5 nf=1 ad='int((nf+1)/2) * W/nf * 0.29' as='int((nf+2)/2) * W/nf * 0.29'
+ pd='2*int((nf+1)/2) * (W/nf + 0.29)' ps='2*int((nf+2)/2) * (W/nf + 0.29)' nrd='0.29 / W' nrs='0.29 / W'
+ sa=0 sb=0 sd=0 mult=1 m=1
XMl10 vn1 ena_b avss avss sky130_fd_pr__nfet_g5v0d10v5 L=2 W=5 nf=1 ad='int((nf+1)/2) * W/nf * 0.29'
+ as='int((nf+2)/2) * W/nf * 0.29' pd='2*int((nf+1)/2) * (W/nf + 0.29)' ps='2*int((nf+2)/2) * (W/nf + 0.29)'
+ nrd='0.29 / W' nrs='0.29 / W' sa=0 sb=0 sd=0 mult=1 m=1
XMl2 vp0 isrc_sel_b avdd avdd sky130_fd_pr__pfet_g5v0d10v5 L=2 W=5 nf=1 ad='int((nf+1)/2) * W/nf * 0.29'
+ as='int((nf+2)/2) * W/nf * 0.29' pd='2*int((nf+1)/2) * (W/nf + 0.29)' ps='2*int((nf+2)/2) * (W/nf + 0.29)'
+ nrd='0.29 / W' nrs='0.29 / W' sa=0 sb=0 sd=0 mult=1 m=1
XMl0 vn0 isrc_sel avss avss sky130_fd_pr__nfet_g5v0d10v5 L=2 W=5 nf=1 ad='int((nf+1)/2) * W/nf * 0.29'
+ as='int((nf+2)/2) * W/nf * 0.29' pd='2*int((nf+1)/2) * (W/nf + 0.29)' ps='2*int((nf+2)/2) * (W/nf + 0.29)'
+ nrd='0.29 / W' nrs='0.29 / W' sa=0 sb=0 sd=0 mult=1 m=1
XMt8 net4 isrc_sel avdd avdd sky130_fd_pr__pfet_g5v0d10v5 L=0.6 W=5 nf=1 ad='int((nf+1)/2) * W/nf * 0.29'
+ as='int((nf+2)/2) * W/nf * 0.29' pd='2*int((nf+1)/2) * (W/nf + 0.29)' ps='2*int((nf+2)/2) * (W/nf + 0.29)'
+ nrd='0.29 / W' nrs='0.29 / W' sa=0 sb=0 sd=0 mult=1 m=1
XMn2 ena_b ena avss avss sky130_fd_pr__nfet_g5v0d10v5 L=1 W=5 nf=1 ad='int((nf+1)/2) * W/nf * 0.29' as='int((nf+2)/2) * W/nf * 0.29'
+ pd='2*int((nf+1)/2) * (W/nf + 0.29)' ps='2*int((nf+2)/2) * (W/nf + 0.29)' nrd='0.29 / W' nrs='0.29 / W'
+ sa=0 sb=0 sd=0 mult=1 m=1
XMp2 ena_b ena avdd avdd sky130_fd_pr__pfet_g5v0d10v5 L=1 W=5 nf=1 ad='int((nf+1)/2) * W/nf * 0.29' as='int((nf+2)/2) * W/nf * 0.29'
+ pd='2*int((nf+1)/2) * (W/nf + 0.29)' ps='2*int((nf+2)/2) * (W/nf + 0.29)' nrd='0.29 / W' nrs='0.29 / W'
+ sa=0 sb=0 sd=0 mult=1 m=1
XMn3 isrc_sel_b isrc_sel avss avss sky130_fd_pr__nfet_g5v0d10v5 L=1 W=5 nf=1 ad='int((nf+1)/2) * W/nf * 0.29'
+ as='int((nf+2)/2) * W/nf * 0.29' pd='2*int((nf+1)/2) * (W/nf + 0.29)' ps='2*int((nf+2)/2) * (W/nf + 0.29)'
+ nrd='0.29 / W' nrs='0.29 / W' sa=0 sb=0 sd=0 mult=1 m=1
XMp3 isrc_sel_b isrc_sel avdd avdd sky130_fd_pr__pfet_g5v0d10v5 L=1 W=5 nf=1 ad='int((nf+1)/2) * W/nf * 0.29'
+ as='int((nf+2)/2) * W/nf * 0.29' pd='2*int((nf+1)/2) * (W/nf + 0.29)' ps='2*int((nf+2)/2) * (W/nf + 0.29)'
+ nrd='0.29 / W' nrs='0.29 / W' sa=0 sb=0 sd=0 mult=1 m=1
XMtst itest vp avdd avdd sky130_fd_pr__pfet_g5v0d10v5 L=4 W=5 nf=1 ad='int((nf+1)/2) * W/nf * 0.29' as='int((nf+2)/2) * W/nf * 0.29'
+ pd='2*int((nf+1)/2) * (W/nf + 0.29)' ps='2*int((nf+2)/2) * (W/nf + 0.29)' nrd='0.29 / W' nrs='0.29 / W'
+ sa=0 sb=0 sd=0 mult=2 m=2
.ends


* expanding   symbol:  rc_osc.sym # of pins=4
** sym_path: xschem/rc_osc.sym
** sch_path: xschem/rc_osc.sch
.subckt rc_osc dvdd out ena dvss
*.ipin dvdd
*.ipin dvss
*.opin out
*.ipin ena
XM1 m in dvss dvss sky130_fd_pr__nfet_01v8 L=0.5 W=1 nf=1 ad='int((nf+1)/2) * W/nf * 0.29' as='int((nf+2)/2) * W/nf * 0.29'
+ pd='2*int((nf+1)/2) * (W/nf + 0.29)' ps='2*int((nf+2)/2) * (W/nf + 0.29)' nrd='0.29 / W' nrs='0.29 / W'
+ sa=0 sb=0 sd=0 mult=2 m=2
XM3 m in dvdd dvdd sky130_fd_pr__pfet_01v8 L=0.5 W=1 nf=1 ad='int((nf+1)/2) * W/nf * 0.29' as='int((nf+2)/2) * W/nf * 0.29'
+ pd='2*int((nf+1)/2) * (W/nf + 0.29)' ps='2*int((nf+2)/2) * (W/nf + 0.29)' nrd='0.29 / W' nrs='0.29 / W'
+ sa=0 sb=0 sd=0 mult=6 m=6
XM2 m n dvss dvss sky130_fd_pr__nfet_01v8 L=1 W=1 nf=1 ad='int((nf+1)/2) * W/nf * 0.29' as='int((nf+2)/2) * W/nf * 0.29'
+ pd='2*int((nf+1)/2) * (W/nf + 0.29)' ps='2*int((nf+2)/2) * (W/nf + 0.29)' nrd='0.29 / W' nrs='0.29 / W'
+ sa=0 sb=0 sd=0 mult=1 m=1
XM4 m n dvdd dvdd sky130_fd_pr__pfet_01v8 L=1 W=1 nf=1 ad='int((nf+1)/2) * W/nf * 0.29' as='int((nf+2)/2) * W/nf * 0.29'
+ pd='2*int((nf+1)/2) * (W/nf + 0.29)' ps='2*int((nf+2)/2) * (W/nf + 0.29)' nrd='0.29 / W' nrs='0.29 / W'
+ sa=0 sb=0 sd=0 mult=3 m=3
XM5 n m dvss dvss sky130_fd_pr__nfet_01v8 L=0.5 W=1 nf=1 ad='int((nf+1)/2) * W/nf * 0.29' as='int((nf+2)/2) * W/nf * 0.29'
+ pd='2*int((nf+1)/2) * (W/nf + 0.29)' ps='2*int((nf+2)/2) * (W/nf + 0.29)' nrd='0.29 / W' nrs='0.29 / W'
+ sa=0 sb=0 sd=0 mult=1 m=1
XM6 n m dvdd dvdd sky130_fd_pr__pfet_01v8 L=0.5 W=1 nf=1 ad='int((nf+1)/2) * W/nf * 0.29' as='int((nf+2)/2) * W/nf * 0.29'
+ pd='2*int((nf+1)/2) * (W/nf + 0.29)' ps='2*int((nf+2)/2) * (W/nf + 0.29)' nrd='0.29 / W' nrs='0.29 / W'
+ sa=0 sb=0 sd=0 mult=3 m=3
XM7 out n dvss dvss sky130_fd_pr__nfet_01v8 L=0.5 W=1 nf=1 ad='int((nf+1)/2) * W/nf * 0.29' as='int((nf+2)/2) * W/nf * 0.29'
+ pd='2*int((nf+1)/2) * (W/nf + 0.29)' ps='2*int((nf+2)/2) * (W/nf + 0.29)' nrd='0.29 / W' nrs='0.29 / W'
+ sa=0 sb=0 sd=0 mult=1 m=1
XM8 out n dvdd dvdd sky130_fd_pr__pfet_01v8 L=0.5 W=1 nf=1 ad='int((nf+1)/2) * W/nf * 0.29' as='int((nf+2)/2) * W/nf * 0.29'
+ pd='2*int((nf+1)/2) * (W/nf + 0.29)' ps='2*int((nf+2)/2) * (W/nf + 0.29)' nrd='0.29 / W' nrs='0.29 / W'
+ sa=0 sb=0 sd=0 mult=3 m=3
XC1 in dvss sky130_fd_pr__cap_mim_m3_1 W=30 L=30 MF=3 m=3
XR1 in net1 dvss sky130_fd_pr__res_xhigh_po W=2 L=1700 mult=1 m=1
XM12 in ena dvdd dvdd sky130_fd_pr__pfet_01v8 L=0.15 W=1 nf=1 ad='int((nf+1)/2) * W/nf * 0.29' as='int((nf+2)/2) * W/nf * 0.29'
+ pd='2*int((nf+1)/2) * (W/nf + 0.29)' ps='2*int((nf+2)/2) * (W/nf + 0.29)' nrd='0.29 / W' nrs='0.29 / W'
+ sa=0 sb=0 sd=0 mult=1 m=1
XC2 in dvss sky130_fd_pr__cap_mim_m3_2 W=30 L=30 MF=3 m=3
XM9 out ena net1 dvss sky130_fd_pr__nfet_01v8 L=0.18 W=1 nf=1 ad='int((nf+1)/2) * W/nf * 0.29' as='int((nf+2)/2) * W/nf * 0.29'
+ pd='2*int((nf+1)/2) * (W/nf + 0.29)' ps='2*int((nf+2)/2) * (W/nf + 0.29)' nrd='0.29 / W' nrs='0.29 / W'
+ sa=0 sb=0 sd=0 mult=1 m=1
XM10 out ena_b net1 dvdd sky130_fd_pr__pfet_01v8 L=0.18 W=1 nf=1 ad='int((nf+1)/2) * W/nf * 0.29' as='int((nf+2)/2) * W/nf * 0.29'
+ pd='2*int((nf+1)/2) * (W/nf + 0.29)' ps='2*int((nf+2)/2) * (W/nf + 0.29)' nrd='0.29 / W' nrs='0.29 / W'
+ sa=0 sb=0 sd=0 mult=1 m=1
XM11 ena_b ena dvss dvss sky130_fd_pr__nfet_01v8 L=0.6 W=1 nf=1 ad='int((nf+1)/2) * W/nf * 0.29' as='int((nf+2)/2) * W/nf * 0.29'
+ pd='2*int((nf+1)/2) * (W/nf + 0.29)' ps='2*int((nf+2)/2) * (W/nf + 0.29)' nrd='0.29 / W' nrs='0.29 / W'
+ sa=0 sb=0 sd=0 mult=1 m=1
XM13 ena_b ena dvdd dvdd sky130_fd_pr__pfet_01v8 L=0.6 W=1 nf=1 ad='int((nf+1)/2) * W/nf * 0.29' as='int((nf+2)/2) * W/nf * 0.29'
+ pd='2*int((nf+1)/2) * (W/nf + 0.29)' ps='2*int((nf+2)/2) * (W/nf + 0.29)' nrd='0.29 / W' nrs='0.29 / W'
+ sa=0 sb=0 sd=0 mult=1 m=1
.ends


* expanding   symbol:  xschem/schmitt_trigger.sym # of pins=4
** sym_path: xschem/schmitt_trigger.sym
** sch_path: xschem/schmitt_trigger.sch
.subckt schmitt_trigger dvdd in out dvss
*.ipin dvdd
*.ipin dvss
*.opin out
*.ipin in
XM1 m in dvss dvss sky130_fd_pr__nfet_01v8 L=0.5 W=1 nf=1 ad='int((nf+1)/2) * W/nf * 0.29' as='int((nf+2)/2) * W/nf * 0.29'
+ pd='2*int((nf+1)/2) * (W/nf + 0.29)' ps='2*int((nf+2)/2) * (W/nf + 0.29)' nrd='0.29 / W' nrs='0.29 / W'
+ sa=0 sb=0 sd=0 mult=2 m=2
XM3 m in dvdd dvdd sky130_fd_pr__pfet_01v8 L=0.5 W=1 nf=1 ad='int((nf+1)/2) * W/nf * 0.29' as='int((nf+2)/2) * W/nf * 0.29'
+ pd='2*int((nf+1)/2) * (W/nf + 0.29)' ps='2*int((nf+2)/2) * (W/nf + 0.29)' nrd='0.29 / W' nrs='0.29 / W'
+ sa=0 sb=0 sd=0 mult=6 m=6
XM2 m out dvss dvss sky130_fd_pr__nfet_01v8 L=0.5 W=1 nf=1 ad='int((nf+1)/2) * W/nf * 0.29' as='int((nf+2)/2) * W/nf * 0.29'
+ pd='2*int((nf+1)/2) * (W/nf + 0.29)' ps='2*int((nf+2)/2) * (W/nf + 0.29)' nrd='0.29 / W' nrs='0.29 / W'
+ sa=0 sb=0 sd=0 mult=1 m=1
XM4 m out dvdd dvdd sky130_fd_pr__pfet_01v8 L=0.5 W=1 nf=1 ad='int((nf+1)/2) * W/nf * 0.29' as='int((nf+2)/2) * W/nf * 0.29'
+ pd='2*int((nf+1)/2) * (W/nf + 0.29)' ps='2*int((nf+2)/2) * (W/nf + 0.29)' nrd='0.29 / W' nrs='0.29 / W'
+ sa=0 sb=0 sd=0 mult=3 m=3
XM5 out m dvss dvss sky130_fd_pr__nfet_01v8 L=0.5 W=1 nf=1 ad='int((nf+1)/2) * W/nf * 0.29' as='int((nf+2)/2) * W/nf * 0.29'
+ pd='2*int((nf+1)/2) * (W/nf + 0.29)' ps='2*int((nf+2)/2) * (W/nf + 0.29)' nrd='0.29 / W' nrs='0.29 / W'
+ sa=0 sb=0 sd=0 mult=1 m=1
XM6 out m dvdd dvdd sky130_fd_pr__pfet_01v8 L=0.5 W=1 nf=1 ad='int((nf+1)/2) * W/nf * 0.29' as='int((nf+2)/2) * W/nf * 0.29'
+ pd='2*int((nf+1)/2) * (W/nf + 0.29)' ps='2*int((nf+2)/2) * (W/nf + 0.29)' nrd='0.29 / W' nrs='0.29 / W'
+ sa=0 sb=0 sd=0 mult=3 m=3
.ends

.end
